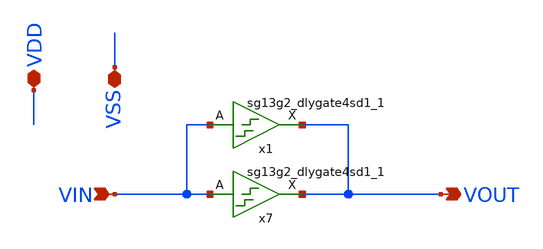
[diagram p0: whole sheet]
** sch_path: QDLL6501-main/schematic/xschem/DLYGATES2.sch
**.subckt DLYGATES2 VIN VDD VSS VOUT
*.ipin VIN
*.iopin VDD
*.iopin VSS
*.opin VOUT
x7 VOUT VIN VDD VSS sg13g2_dlygate4sd1_1
x1 VOUT VIN VDD VSS sg13g2_dlygate4sd1_1
**.ends

* expanding   symbol:  sg13g2_stdcells/sg13g2_dlygate4sd1_1.sym # of pins=2
** sym_path: sg13g2_stdcells/sg13g2_dlygate4sd1_1.sym
** sch_path: sg13g2_stdcells/sg13g2_dlygate4sd1_1.sch
.subckt sg13g2_dlygate4sd1_1 X A VDD VSS
*.ipin A
*.opin X
*.iopin VDD
*.iopin VSS
XM1 net2 A VSS VSS sg13_lv_nmos w=420.00n l=130.00n ng=1 m=1 mm_ok=1
XM2 net1 net2 VSS VSS sg13_lv_nmos w=420.00n l=130.00n ng=1 m=1 mm_ok=1
XM3 net3 net1 VSS VSS sg13_lv_nmos w=420.00n l=130.00n ng=1 m=1 mm_ok=1
XM4 X net3 VSS VSS sg13_lv_nmos w=740.00n l=130.00n ng=1 m=1 mm_ok=1
XM5 net2 A VDD VDD sg13_lv_pmos w=420.00n l=130.00n ng=1 m=1 mm_ok=1
XM6 net1 net2 VDD VDD sg13_lv_pmos w=1.000u l=130.00n ng=1 m=1 mm_ok=1
XM7 net3 net1 VDD VDD sg13_lv_pmos w=1.000u l=130.00n ng=1 m=1 mm_ok=1
XM8 X net3 VDD VDD sg13_lv_pmos w=1.12u l=130.00n ng=1 m=1 mm_ok=1
.ends

.end
